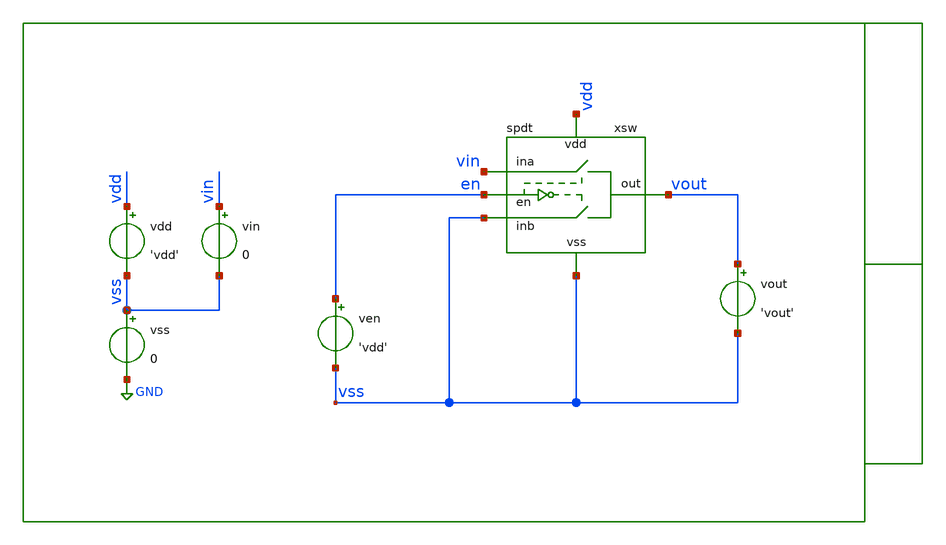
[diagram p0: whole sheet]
** sch_path: xschem/tb/spdt/spdt/dc_spdt_ron.sch
**.subckt dc_spdt_ron
vdd vdd vss 'vdd'
vss vss GND 0
ven en vss 'vdd'
xsw vout en vdd vss vss vin spdt
vin vin vss 0
vout vout vss 'vout'
**** begin user architecture code

* Control

.param vdd = 3.3

.param vout = 'vdd/2'
.param vin = 'vdd'

.temp 27


.control
save all

dc vin 0.05 3.3 0.0033

let vdelta = abs( v(vin) - v(vout) )
let iout = abs(vout#branch)

let rsw = vdelta/iout

meas dc rsw_max max rsw
meas dc rsw_min min rsw

print rsw_max

gnuplot p1 rsw

set wr_singlescale
set wr_vecnames
wrdata data.csv rsw

.endc
.end


 * Model Corners

.include $::CORNERS/ngspice/tt.spice
*.include $::CORNERS/ngspice/ff.spice
*.include $::CORNERS/ngspice/ss.spice
*.include $::CORNERS/ngspice/sf.spice
*.include $::CORNERS/ngspice/fs.spice

**** end user architecture code
**.ends

* expanding   symbol:  sch/spdt/spdt/spdt.sym # of pins=6
** sym_path: xschem/sch/spdt/spdt/spdt.sym
** sch_path: xschem/sch/spdt/spdt/spdt.sch
.subckt spdt out en vdd inb vss ina
*.ipin en
*.iopin vss
*.iopin vdd
*.iopin ina
*.iopin out
*.iopin inb
XMI1 enb_buf en vss vss nfet_06v0 L=1u W=4u nf=1 ad='int((nf+1)/2) * W/nf * 0.18u' as='int((nf+2)/2) * W/nf * 0.18u'
+ pd='2*int((nf+1)/2) * (W/nf + 0.18u)' ps='2*int((nf+2)/2) * (W/nf + 0.18u)' nrd='0.18u / W' nrs='0.18u / W'
+ sa=0 sb=0 sd=0 m=1 par=1
XMI2 en_buf enb_buf vss vss nfet_06v0 L=1u W=4u nf=1 ad='int((nf+1)/2) * W/nf * 0.18u' as='int((nf+2)/2) * W/nf * 0.18u'
+ pd='2*int((nf+1)/2) * (W/nf + 0.18u)' ps='2*int((nf+2)/2) * (W/nf + 0.18u)' nrd='0.18u / W' nrs='0.18u / W'
+ sa=0 sb=0 sd=0 m=1 par=1
XMI3 enb_buf en vdd vdd pfet_06v0 L=1u W=8u nf=1 ad='int((nf+1)/2) * W/nf * 0.18u' as='int((nf+2)/2) * W/nf * 0.18u'
+ pd='2*int((nf+1)/2) * (W/nf + 0.18u)' ps='2*int((nf+2)/2) * (W/nf + 0.18u)' nrd='0.18u / W' nrs='0.18u / W'
+ sa=0 sb=0 sd=0 m=1 par=1
XMI4 en_buf enb_buf vdd vdd pfet_06v0 L=1u W=8u nf=1 ad='int((nf+1)/2) * W/nf * 0.18u' as='int((nf+2)/2) * W/nf * 0.18u'
+ pd='2*int((nf+1)/2) * (W/nf + 0.18u)' ps='2*int((nf+2)/2) * (W/nf + 0.18u)' nrd='0.18u / W' nrs='0.18u / W'
+ sa=0 sb=0 sd=0 m=1 par=1
XM2 inb en_buf out vdd pfet_06v0 L=1u W=64u nf=8 ad='int((nf+1)/2) * W/nf * 0.18u' as='int((nf+2)/2) * W/nf * 0.18u'
+ pd='2*int((nf+1)/2) * (W/nf + 0.18u)' ps='2*int((nf+2)/2) * (W/nf + 0.18u)' nrd='0.18u / W' nrs='0.18u / W'
+ sa=0 sb=0 sd=0 m=1 par=1
XM1 inb enb_buf out vss nfet_06v0 L=1u W=32u nf=4 ad='int((nf+1)/2) * W/nf * 0.18u' as='int((nf+2)/2) * W/nf * 0.18u'
+ pd='2*int((nf+1)/2) * (W/nf + 0.18u)' ps='2*int((nf+2)/2) * (W/nf + 0.18u)' nrd='0.18u / W' nrs='0.18u / W'
+ sa=0 sb=0 sd=0 m=1 par=1
XM3 ina en_buf out vss nfet_06v0 L=1u W=32u nf=4 ad='int((nf+1)/2) * W/nf * 0.18u' as='int((nf+2)/2) * W/nf * 0.18u'
+ pd='2*int((nf+1)/2) * (W/nf + 0.18u)' ps='2*int((nf+2)/2) * (W/nf + 0.18u)' nrd='0.18u / W' nrs='0.18u / W'
+ sa=0 sb=0 sd=0 m=1 par=1
XM4 ina enb_buf out vdd pfet_06v0 L=1u W=64u nf=8 ad='int((nf+1)/2) * W/nf * 0.18u' as='int((nf+2)/2) * W/nf * 0.18u'
+ pd='2*int((nf+1)/2) * (W/nf + 0.18u)' ps='2*int((nf+2)/2) * (W/nf + 0.18u)' nrd='0.18u / W' nrs='0.18u / W'
+ sa=0 sb=0 sd=0 m=1 par=1
.ends

.GLOBAL GND
.end
